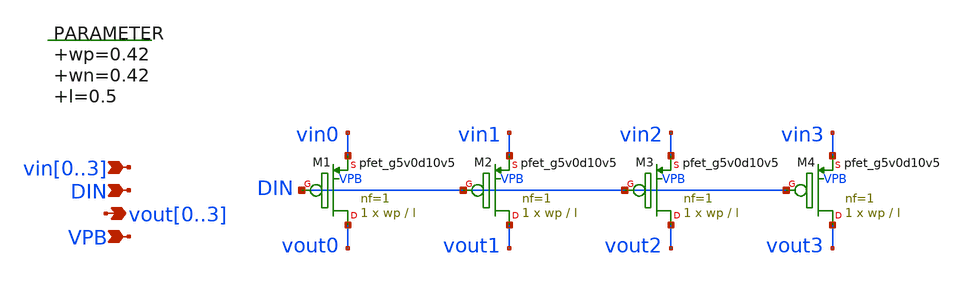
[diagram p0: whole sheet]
** sch_path: xschem/switch_pmos_1g_4o.sch
**.subckt switch_pmos_1g_4o vin0,vin1,vin2,vin3 vout0,vout1,vout2,vout3 VPB DIN
*.ipin vin0,vin1,vin2,vin3
*.opin vout0,vout1,vout2,vout3
*.ipin VPB
*.ipin DIN
.param wp=0.42 wn=0.42 l=0.5

XM1 vout0 DIN vin0 VPB sky130_fd_pr__pfet_g5v0d10v5 L=l W=wp nf=1 ad='int((nf+1)/2) * W/nf * 0.29' as='int((nf+2)/2) * W/nf * 0.29'
+ pd='2*int((nf+1)/2) * (W/nf + 0.29)' ps='2*int((nf+2)/2) * (W/nf + 0.29)' nrd='0.29 / W' nrs='0.29 / W'
+ sa=0 sb=0 sd=0 mult=1 m=1
XM2 vout1 DIN vin1 VPB sky130_fd_pr__pfet_g5v0d10v5 L=l W=wp nf=1 ad='int((nf+1)/2) * W/nf * 0.29' as='int((nf+2)/2) * W/nf * 0.29'
+ pd='2*int((nf+1)/2) * (W/nf + 0.29)' ps='2*int((nf+2)/2) * (W/nf + 0.29)' nrd='0.29 / W' nrs='0.29 / W'
+ sa=0 sb=0 sd=0 mult=1 m=1
XM3 vout2 DIN vin2 VPB sky130_fd_pr__pfet_g5v0d10v5 L=l W=wp nf=1 ad='int((nf+1)/2) * W/nf * 0.29' as='int((nf+2)/2) * W/nf * 0.29'
+ pd='2*int((nf+1)/2) * (W/nf + 0.29)' ps='2*int((nf+2)/2) * (W/nf + 0.29)' nrd='0.29 / W' nrs='0.29 / W'
+ sa=0 sb=0 sd=0 mult=1 m=1
XM4 vout3 DIN vin3 VPB sky130_fd_pr__pfet_g5v0d10v5 L=l W=wp nf=1 ad='int((nf+1)/2) * W/nf * 0.29' as='int((nf+2)/2) * W/nf * 0.29'
+ pd='2*int((nf+1)/2) * (W/nf + 0.29)' ps='2*int((nf+2)/2) * (W/nf + 0.29)' nrd='0.29 / W' nrs='0.29 / W'
+ sa=0 sb=0 sd=0 mult=1 m=1
**.ends
.end
